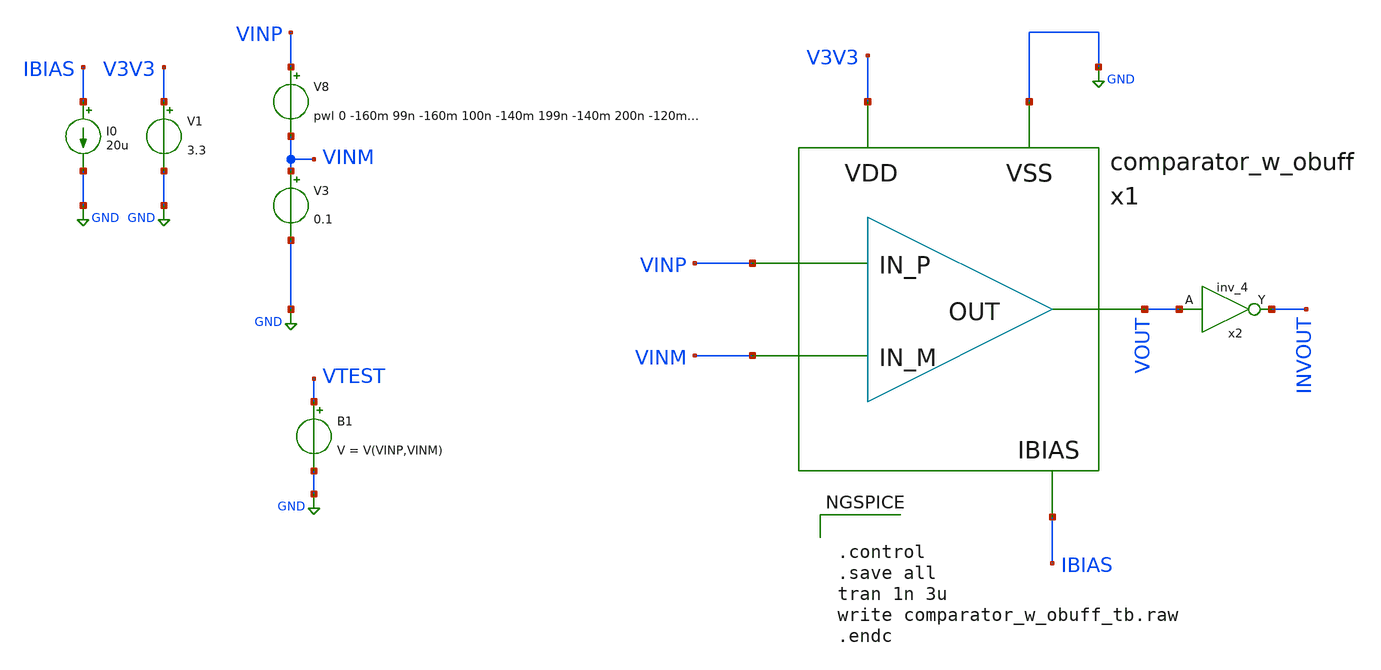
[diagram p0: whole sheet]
** sch_path: images/iic-osic-tools/addons/examples/open-pmic/design/comparator/comparator_w_obuff_tb.sch
**.subckt comparator_w_obuff_tb
V1 V3V3 GND 3.3
I0 IBIAS GND 20u
V3 VINM GND 0.1
x2 VOUT GND GND V3V3 V3V3 INVOUT sky130_fd_sc_hvl__inv_4
B1 VTEST GND V = V(VINP,VINM)
x1 IBIAS V3V3 VINM VINP VOUT GND comparator_w_obuff
V8 VINP VINM pwl 0 -160m 99n -160m 100n -140m 199n -140m 200n -120m 299n -120m 300n -100m 399n -100m
+ 400n -80m 499n -80m 500n -60m 599n -60m 600n -40m 699n -40m 700n -20m 799n -20m 800n 0 899n 0 900n 20m
+ 999n 20m 1u 40m 1.099u 40m 1.1u 42m 1.199u 42m 1.2u 44m 1.299u 44m 1.3u 46m 1.399u 46m 1.4u 48m 1.499u
+ 48m 1.5u 50m 1.599u 50m 1.6u 52m 1.699u 52m 1.7u 54m 1.799u 54m 1.8u 56m 1.899u 56m 1.9u 58m 1.999u 58m
+ 2u 60m 2.099u 60m 2.1u 80m 2.199u 80m 2.2u 100m 2.299u 100m 2.3u 120m 2.399u 120m 2.4u 140m 2.499u
+ 140m 2.5u 160m 2.599u 160m
**** begin user architecture code

.include $::SKYWATER_MODELS/cells/nfet_01v8/sky130_fd_pr__nfet_01v8__tt.corner.spice
.include $::SKYWATER_MODELS/cells/nfet_01v8_lvt/sky130_fd_pr__nfet_01v8_lvt__tt.corner.spice
.include $::SKYWATER_MODELS/cells/pfet_01v8/sky130_fd_pr__pfet_01v8__tt.corner.spice
.include $::SKYWATER_MODELS/cells/nfet_03v3_nvt/sky130_fd_pr__nfet_03v3_nvt__tt.corner.spice
.include $::SKYWATER_MODELS/cells/nfet_05v0_nvt/sky130_fd_pr__nfet_05v0_nvt__tt.corner.spice
.include $::SKYWATER_MODELS/cells/esd_nfet_01v8/sky130_fd_pr__esd_nfet_01v8__tt.corner.spice
.include $::SKYWATER_MODELS/cells/pfet_01v8_lvt/sky130_fd_pr__pfet_01v8_lvt__tt.corner.spice
.include $::SKYWATER_MODELS/cells/pfet_01v8_hvt/sky130_fd_pr__pfet_01v8_hvt__tt.corner.spice
.include $::SKYWATER_MODELS/cells/esd_pfet_g5v0d10v5/sky130_fd_pr__esd_pfet_g5v0d10v5__tt.corner.spice
.include $::SKYWATER_MODELS/cells/pfet_g5v0d10v5/sky130_fd_pr__pfet_g5v0d10v5__tt.corner.spice
.include $::SKYWATER_MODELS/cells/pfet_g5v0d16v0/sky130_fd_pr__pfet_g5v0d16v0__tt.corner.spice
.include $::SKYWATER_MODELS/cells/nfet_g5v0d10v5/sky130_fd_pr__nfet_g5v0d10v5__tt.corner.spice
.include $::SKYWATER_MODELS/cells/nfet_g5v0d16v0/sky130_fd_pr__nfet_g5v0d16v0__tt_discrete.corner.spice
.include $::SKYWATER_MODELS/cells/esd_nfet_g5v0d10v5/sky130_fd_pr__esd_nfet_g5v0d10v5__tt.corner.spice
.include $::SKYWATER_MODELS/models/corners/tt/nonfet.spice
* Mismatch parameters
.include $::SKYWATER_MODELS/cells/nfet_01v8/sky130_fd_pr__nfet_01v8__mismatch.corner.spice
.include $::SKYWATER_MODELS/cells/pfet_01v8/sky130_fd_pr__pfet_01v8__mismatch.corner.spice
.include $::SKYWATER_MODELS/cells/nfet_01v8_lvt/sky130_fd_pr__nfet_01v8_lvt__mismatch.corner.spice
.include $::SKYWATER_MODELS/cells/pfet_01v8_lvt/sky130_fd_pr__pfet_01v8_lvt__mismatch.corner.spice
.include $::SKYWATER_MODELS/cells/pfet_01v8_hvt/sky130_fd_pr__pfet_01v8_hvt__mismatch.corner.spice
.include $::SKYWATER_MODELS/cells/nfet_g5v0d10v5/sky130_fd_pr__nfet_g5v0d10v5__mismatch.corner.spice
.include $::SKYWATER_MODELS/cells/pfet_g5v0d10v5/sky130_fd_pr__pfet_g5v0d10v5__mismatch.corner.spice
.include $::SKYWATER_MODELS/cells/nfet_05v0_nvt/sky130_fd_pr__nfet_05v0_nvt__mismatch.corner.spice
.include $::SKYWATER_MODELS/cells/nfet_03v3_nvt/sky130_fd_pr__nfet_03v3_nvt__mismatch.corner.spice
* Resistor$::SKYWATER_MODELS/Capacitor
.include $::SKYWATER_MODELS/models/r+c/res_typical__cap_typical.spice
.include $::SKYWATER_MODELS/models/r+c/res_typical__cap_typical__lin.spice
* Special cells
.include $::SKYWATER_MODELS/models/corners/tt/specialized_cells.spice
* All models
.include $::SKYWATER_MODELS/models/all.spice
* Corner
.include $::SKYWATER_MODELS/models/corners/tt/rf.spice



.control
.save all
tran 1n 3u
write comparator_w_obuff_tb.raw
.endc


**** end user architecture code
**.ends
.GLOBAL GND
**** begin user architecture code
[sky130_models]
**** end user architecture code
.end
